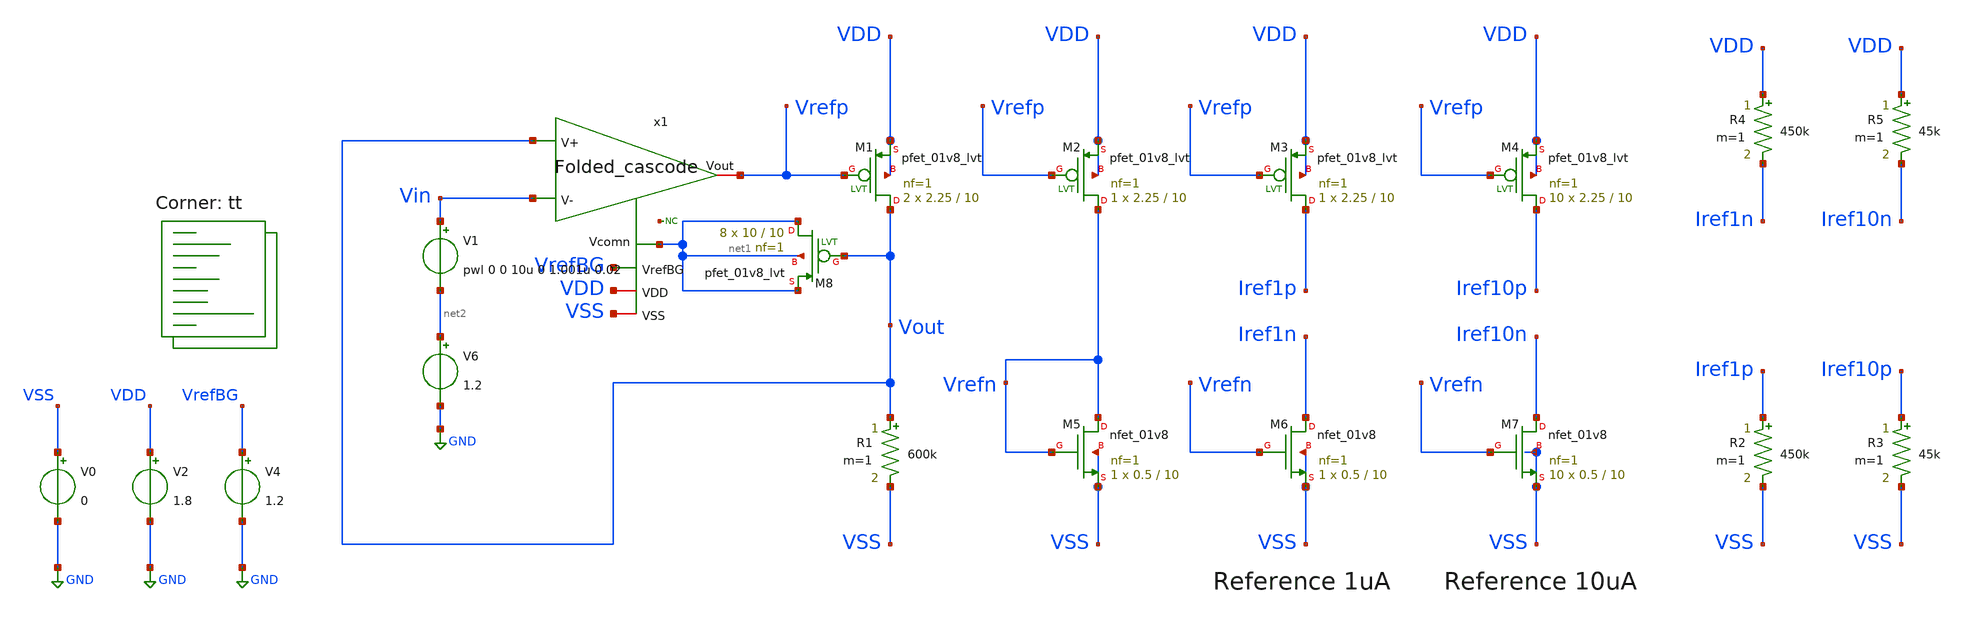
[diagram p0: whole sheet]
** sch_path: openfasoc/generators/curref-gen/sch/Current_reference_generator_Tran.sch
**.subckt Current_reference_generator_Tran
XM1 Vout Vrefp VDD VDD sky130_fd_pr__pfet_01v8_lvt L=10 W=2.25 nf=1 ad='int((1 + 1)/2) * 2.25 / 1 * 0.29'
+ as='int((1 + 2)/2) * 2.25 / 1 * 0.29' pd='2*int((1 + 1)/2) * (2.25 / 1 + 0.29)' ps='2*int((1 + 2)/2) * (2.25 / 1 + 0.29)'
+ nrd='0.29 / 2.25 ' nrs='0.29 / 2.25 ' sa=0 sb=0 sd=0 mult=2 m=2
R1 Vout VSS 600k m=1
XM2 Vrefn Vrefp VDD VDD sky130_fd_pr__pfet_01v8_lvt L=10 W=2.25 nf=1 ad='int((1 + 1)/2) * 2.25 / 1 * 0.29'
+ as='int((1 + 2)/2) * 2.25 / 1 * 0.29' pd='2*int((1 + 1)/2) * (2.25 / 1 + 0.29)' ps='2*int((1 + 2)/2) * (2.25 / 1 + 0.29)'
+ nrd='0.29 / 2.25 ' nrs='0.29 / 2.25 ' sa=0 sb=0 sd=0 mult=1 m=1
XM5 Vrefn Vrefn VSS VSS sky130_fd_pr__nfet_01v8 L=10 W=0.5 nf=1 ad='int((nf+1)/2) * W/nf * 0.29' as='int((nf+2)/2) * W/nf * 0.29'
+ pd='2*int((nf+1)/2) * (W/nf + 0.29)' ps='2*int((nf+2)/2) * (W/nf + 0.29)' nrd='0.29 / W' nrs='0.29 / W'
+ sa=0 sb=0 sd=0 mult=1 m=1
XM6 Iref1n Vrefn VSS VSS sky130_fd_pr__nfet_01v8 L=10 W=0.5 nf=1 ad='int((nf+1)/2) * W/nf * 0.29' as='int((nf+2)/2) * W/nf * 0.29'
+ pd='2*int((nf+1)/2) * (W/nf + 0.29)' ps='2*int((nf+2)/2) * (W/nf + 0.29)' nrd='0.29 / W' nrs='0.29 / W'
+ sa=0 sb=0 sd=0 mult=1 m=1
XM3 Iref1p Vrefp VDD VDD sky130_fd_pr__pfet_01v8_lvt L=10 W=2.25 nf=1 ad='int((1 + 1)/2) * 2.25 / 1 * 0.29'
+ as='int((1 + 2)/2) * 2.25 / 1 * 0.29' pd='2*int((1 + 1)/2) * (2.25 / 1 + 0.29)' ps='2*int((1 + 2)/2) * (2.25 / 1 + 0.29)'
+ nrd='0.29 / 2.25 ' nrs='0.29 / 2.25 ' sa=0 sb=0 sd=0 mult=1 m=1
XM7 Iref10n Vrefn VSS VSS sky130_fd_pr__nfet_01v8 L=10 W=0.5 nf=1 ad='int((nf+1)/2) * W/nf * 0.29' as='int((nf+2)/2) * W/nf * 0.29'
+ pd='2*int((nf+1)/2) * (W/nf + 0.29)' ps='2*int((nf+2)/2) * (W/nf + 0.29)' nrd='0.29 / W' nrs='0.29 / W'
+ sa=0 sb=0 sd=0 mult=10 m=10
XM4 Iref10p Vrefp VDD VDD sky130_fd_pr__pfet_01v8_lvt L=10 W=2.25 nf=1 ad='int((1 + 1)/2) * 2.25 / 1 * 0.29'
+ as='int((1 + 2)/2) * 2.25 / 1 * 0.29' pd='2*int((1 + 1)/2) * (2.25 / 1 + 0.29)' ps='2*int((1 + 2)/2) * (2.25 / 1 + 0.29)'
+ nrd='0.29 / 2.25 ' nrs='0.29 / 2.25 ' sa=0 sb=0 sd=0 mult=10 m=10
V0 VSS GND 0
V2 VDD GND 1.8
V4 VrefBG GND 1.2
R2 Iref1p VSS 450k m=1
R3 Iref10p VSS 45k m=1
R4 VDD Iref1n 450k m=1
R5 VDD Iref10n 45k m=1
V6 net2 GND 1.2
x1 Vrefp Vout Vin VrefBG VDD VSS net1 Folded_cascode
XM8 net1 Vout net1 net1 sky130_fd_pr__pfet_01v8_lvt L=10 W=10 nf=1 ad='int((1 + 1)/2) * 10 / 1 * 0.29'
+ as='int((1 + 2)/2) * 10 / 1 * 0.29' pd='2*int((1 + 1)/2) * (10 / 1 + 0.29)' ps='2*int((1 + 2)/2) * (10 / 1 + 0.29)'
+ nrd='0.29 / 10 ' nrs='0.29 / 10 ' sa=0 sb=0 sd=0 mult=8 m=8
V1 Vin net2 pwl 0 0 10u 0 1.001u 0.02
* noconn #net3
**** begin user architecture code



.param VDD=1.8
.param VrefBG=1.2

.save

.control

    op
    show

    write Current_reference_generator_Tran.raw
    set appendwrite

    * run tran simulation
    tran 1n 20u

    plot v(Vout) v(Vin)
    plot i(Iref1n)

    write Current_reference_generator_Tran.raw
.endc



.lib $::SKYWATER_MODELS/sky130.lib.spice tt
**** end user architecture code
**.ends

* expanding   symbol:  /foss/designs/Folded_cascode/Folded_cascode.sym # of pins=7
** sym_path: openfasoc/generators/curref-gen/sch/Folded_cascode.sym
** sch_path: openfasoc/generators/curref-gen/sch/Folded_cascode.sch
.subckt Folded_cascode Vout V+ V- VrefBG VDD VSS Vcomn
*.ipin V+
*.ipin V-
*.ipin VrefBG
*.iopin VDD
*.iopin VSS
*.iopin Vout
*.iopin Vcomn
XM6 net2 V- net5 net5 sky130_fd_pr__nfet_01v8 L=1 W=1 nf=1 ad='int((nf+1)/2) * W/nf * 0.29' as='int((nf+2)/2) * W/nf * 0.29'
+ pd='2*int((nf+1)/2) * (W/nf + 0.29)' ps='2*int((nf+2)/2) * (W/nf + 0.29)' nrd='0.29 / W' nrs='0.29 / W'
+ sa=0 sb=0 sd=0 mult=20 m=20
XM7 Vout VB2 Vcomn VSS sky130_fd_pr__nfet_01v8 L=3 W=1 nf=1 ad='int((nf+1)/2) * W/nf * 0.29' as='int((nf+2)/2) * W/nf * 0.29'
+ pd='2*int((nf+1)/2) * (W/nf + 0.29)' ps='2*int((nf+2)/2) * (W/nf + 0.29)' nrd='0.29 / W' nrs='0.29 / W'
+ sa=0 sb=0 sd=0 mult=5 m=5
XM8 net4 VB2 net3 VSS sky130_fd_pr__nfet_01v8 L=3 W=1 nf=1 ad='int((nf+1)/2) * W/nf * 0.29' as='int((nf+2)/2) * W/nf * 0.29'
+ pd='2*int((nf+1)/2) * (W/nf + 0.29)' ps='2*int((nf+2)/2) * (W/nf + 0.29)' nrd='0.29 / W' nrs='0.29 / W'
+ sa=0 sb=0 sd=0 mult=5 m=5
XM9 Vcomn VP VSS VSS sky130_fd_pr__nfet_01v8 L=6.5 W=0.5 nf=1 ad='int((nf+1)/2) * W/nf * 0.29' as='int((nf+2)/2) * W/nf * 0.29'
+ pd='2*int((nf+1)/2) * (W/nf + 0.29)' ps='2*int((nf+2)/2) * (W/nf + 0.29)' nrd='0.29 / W' nrs='0.29 / W'
+ sa=0 sb=0 sd=0 mult=5 m=5
XM10 net3 VP VSS VSS sky130_fd_pr__nfet_01v8 L=6.5 W=0.5 nf=1 ad='int((nf+1)/2) * W/nf * 0.29' as='int((nf+2)/2) * W/nf * 0.29'
+ pd='2*int((nf+1)/2) * (W/nf + 0.29)' ps='2*int((nf+2)/2) * (W/nf + 0.29)' nrd='0.29 / W' nrs='0.29 / W'
+ sa=0 sb=0 sd=0 mult=5 m=5
XM11 net5 VP VSS VSS sky130_fd_pr__nfet_01v8 L=6.5 W=0.5 nf=1 ad='int((nf+1)/2) * W/nf * 0.29' as='int((nf+2)/2) * W/nf * 0.29'
+ pd='2*int((nf+1)/2) * (W/nf + 0.29)' ps='2*int((nf+2)/2) * (W/nf + 0.29)' nrd='0.29 / W' nrs='0.29 / W'
+ sa=0 sb=0 sd=0 mult=10 m=10
XM1 net1 V+ net5 net5 sky130_fd_pr__nfet_01v8 L=1 W=1 nf=1 ad='int((nf+1)/2) * W/nf * 0.29' as='int((nf+2)/2) * W/nf * 0.29'
+ pd='2*int((nf+1)/2) * (W/nf + 0.29)' ps='2*int((nf+2)/2) * (W/nf + 0.29)' nrd='0.29 / W' nrs='0.29 / W'
+ sa=0 sb=0 sd=0 mult=20 m=20
XM12 VP VP VSS VSS sky130_fd_pr__nfet_01v8 L=6.5 W=0.5 nf=1 ad='int((nf+1)/2) * W/nf * 0.29' as='int((nf+2)/2) * W/nf * 0.29'
+ pd='2*int((nf+1)/2) * (W/nf + 0.29)' ps='2*int((nf+2)/2) * (W/nf + 0.29)' nrd='0.29 / W' nrs='0.29 / W'
+ sa=0 sb=0 sd=0 mult=1 m=1
XM13 net6 VP VSS VSS sky130_fd_pr__nfet_01v8 L=6.5 W=0.5 nf=1 ad='int((nf+1)/2) * W/nf * 0.29' as='int((nf+2)/2) * W/nf * 0.29'
+ pd='2*int((nf+1)/2) * (W/nf + 0.29)' ps='2*int((nf+2)/2) * (W/nf + 0.29)' nrd='0.29 / W' nrs='0.29 / W'
+ sa=0 sb=0 sd=0 mult=1 m=1
XM17 VB2 VB2 VSS VSS sky130_fd_pr__nfet_01v8 L=18 W=0.42 nf=1 ad='int((nf+1)/2) * W/nf * 0.29' as='int((nf+2)/2) * W/nf * 0.29'
+ pd='2*int((nf+1)/2) * (W/nf + 0.29)' ps='2*int((nf+2)/2) * (W/nf + 0.29)' nrd='0.29 / W' nrs='0.29 / W'
+ sa=0 sb=0 sd=0 mult=1 m=1
XM18 VB2 net6 VDD VDD sky130_fd_pr__pfet_01v8_lvt L=6 W=0.5 nf=1 ad='int((1 + 1)/2) * 0.5 / 1 * 0.29'
+ as='int((1 + 2)/2) * 0.5 / 1 * 0.29' pd='2*int((1 + 1)/2) * (0.5 / 1 + 0.29)' ps='2*int((1 + 2)/2) * (0.5 / 1 + 0.29)'
+ nrd='0.29 / 0.5 ' nrs='0.29 / 0.5 ' sa=0 sb=0 sd=0 mult=4 m=4
XM15 net6 net6 VDD VDD sky130_fd_pr__pfet_01v8_lvt L=6 W=0.5 nf=1 ad='int((1 + 1)/2) * 0.5 / 1 * 0.29'
+ as='int((1 + 2)/2) * 0.5 / 1 * 0.29' pd='2*int((1 + 1)/2) * (0.5 / 1 + 0.29)' ps='2*int((1 + 2)/2) * (0.5 / 1 + 0.29)'
+ nrd='0.29 / 0.5 ' nrs='0.29 / 0.5 ' sa=0 sb=0 sd=0 mult=4 m=4
XM3 net1 net4 VDD VDD sky130_fd_pr__pfet_01v8_lvt L=3 W=1 nf=1 ad='int((1 + 1)/2) * 1 / 1 * 0.29' as='int((1 + 2)/2) * 1 / 1 * 0.29'
+ pd='2*int((1 + 1)/2) * (1 / 1 + 0.29)' ps='2*int((1 + 2)/2) * (1 / 1 + 0.29)' nrd='0.29 / 1 ' nrs='0.29 / 1 '
+ sa=0 sb=0 sd=0 mult=6 m=6
XM2 net2 net4 VDD VDD sky130_fd_pr__pfet_01v8_lvt L=3 W=1 nf=1 ad='int((1 + 1)/2) * 1 / 1 * 0.29' as='int((1 + 2)/2) * 1 / 1 * 0.29'
+ pd='2*int((1 + 1)/2) * (1 / 1 + 0.29)' ps='2*int((1 + 2)/2) * (1 / 1 + 0.29)' nrd='0.29 / 1 ' nrs='0.29 / 1 '
+ sa=0 sb=0 sd=0 mult=6 m=6
XM5 net4 VB1 net1 VDD sky130_fd_pr__pfet_01v8_lvt L=1.5 W=1 nf=1 ad='int((1 + 1)/2) * 1 / 1 * 0.29' as='int((1 + 2)/2) * 1 / 1 * 0.29'
+ pd='2*int((1 + 1)/2) * (1 / 1 + 0.29)' ps='2*int((1 + 2)/2) * (1 / 1 + 0.29)' nrd='0.29 / 1 ' nrs='0.29 / 1 '
+ sa=0 sb=0 sd=0 mult=10 m=10
XM16 Vout VB1 net2 VDD sky130_fd_pr__pfet_01v8_lvt L=1.5 W=1 nf=1 ad='int((1 + 1)/2) * 1 / 1 * 0.29'
+ as='int((1 + 2)/2) * 1 / 1 * 0.29' pd='2*int((1 + 1)/2) * (1 / 1 + 0.29)' ps='2*int((1 + 2)/2) * (1 / 1 + 0.29)'
+ nrd='0.29 / 1 ' nrs='0.29 / 1 ' sa=0 sb=0 sd=0 mult=10 m=10
XM4 VP VB1 VDD VDD sky130_fd_pr__pfet_01v8_lvt L=6 W=0.5 nf=1 ad='int((1 + 1)/2) * 0.5 / 1 * 0.29' as='int((1 + 2)/2) * 0.5 / 1 * 0.29'
+ pd='2*int((1 + 1)/2) * (0.5 / 1 + 0.29)' ps='2*int((1 + 2)/2) * (0.5 / 1 + 0.29)' nrd='0.29 / 0.5 ' nrs='0.29 / 0.5 '
+ sa=0 sb=0 sd=0 mult=1 m=1
XM14 VB1 VB1 VDD VDD sky130_fd_pr__pfet_01v8_lvt L=6 W=0.5 nf=1 ad='int((1 + 1)/2) * 0.5 / 1 * 0.29'
+ as='int((1 + 2)/2) * 0.5 / 1 * 0.29' pd='2*int((1 + 1)/2) * (0.5 / 1 + 0.29)' ps='2*int((1 + 2)/2) * (0.5 / 1 + 0.29)'
+ nrd='0.29 / 0.5 ' nrs='0.29 / 0.5 ' sa=0 sb=0 sd=0 mult=1 m=1
XM19 VB1 VrefBG VSS VSS sky130_fd_pr__nfet_01v8 L=18 W=0.45 nf=1 ad='int((nf+1)/2) * W/nf * 0.29' as='int((nf+2)/2) * W/nf * 0.29'
+ pd='2*int((nf+1)/2) * (W/nf + 0.29)' ps='2*int((nf+2)/2) * (W/nf + 0.29)' nrd='0.29 / W' nrs='0.29 / W'
+ sa=0 sb=0 sd=0 mult=1 m=1
.ends

.GLOBAL GND
.end
